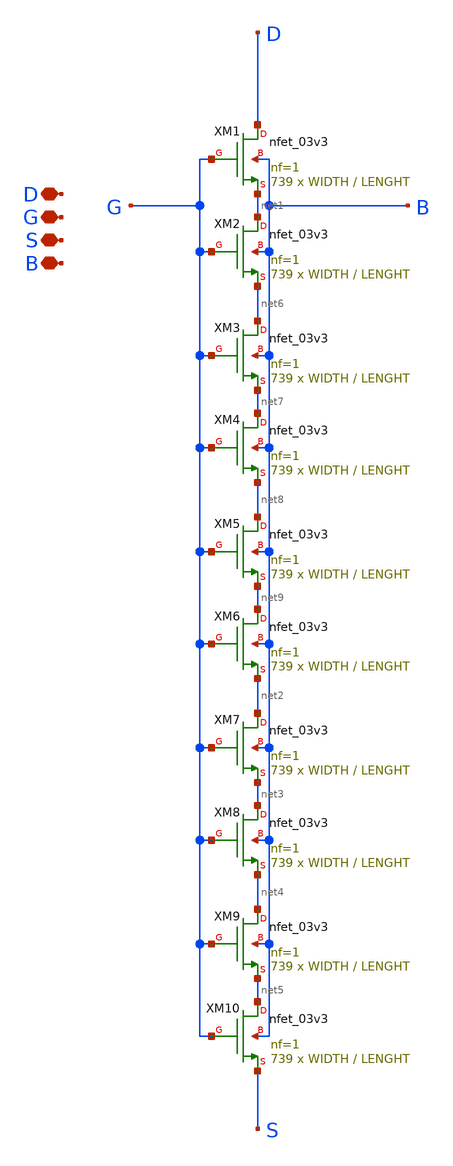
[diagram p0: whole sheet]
** sch_path: New_Extraction/Association/M2_ass.sch
**.subckt M2_ass D G S B
*.iopin D
*.iopin G
*.iopin S
*.iopin B
XM1 D G net1 B nfet_03v3 L=LENGHT W=WIDTH nf=1 ad='int((nf+1)/2) * W/nf * 0.18u' as='int((nf+2)/2) * W/nf * 0.18u'
+ pd='2*int((nf+1)/2) * (W/nf + 0.18u)' ps='2*int((nf+2)/2) * (W/nf + 0.18u)' nrd='0.18u / W' nrs='0.18u / W'
+ sa=0 sb=0 sd=0 m=739
XM2 net1 G net6 B nfet_03v3 L=LENGHT W=WIDTH nf=1 ad='int((nf+1)/2) * W/nf * 0.18u' as='int((nf+2)/2) * W/nf * 0.18u'
+ pd='2*int((nf+1)/2) * (W/nf + 0.18u)' ps='2*int((nf+2)/2) * (W/nf + 0.18u)' nrd='0.18u / W' nrs='0.18u / W'
+ sa=0 sb=0 sd=0 m=739
XM3 net6 G net7 B nfet_03v3 L=LENGHT W=WIDTH nf=1 ad='int((nf+1)/2) * W/nf * 0.18u' as='int((nf+2)/2) * W/nf * 0.18u'
+ pd='2*int((nf+1)/2) * (W/nf + 0.18u)' ps='2*int((nf+2)/2) * (W/nf + 0.18u)' nrd='0.18u / W' nrs='0.18u / W'
+ sa=0 sb=0 sd=0 m=739
XM4 net7 G net8 B nfet_03v3 L=LENGHT W=WIDTH nf=1 ad='int((nf+1)/2) * W/nf * 0.18u' as='int((nf+2)/2) * W/nf * 0.18u'
+ pd='2*int((nf+1)/2) * (W/nf + 0.18u)' ps='2*int((nf+2)/2) * (W/nf + 0.18u)' nrd='0.18u / W' nrs='0.18u / W'
+ sa=0 sb=0 sd=0 m=739
XM5 net8 G net9 B nfet_03v3 L=LENGHT W=WIDTH nf=1 ad='int((nf+1)/2) * W/nf * 0.18u' as='int((nf+2)/2) * W/nf * 0.18u'
+ pd='2*int((nf+1)/2) * (W/nf + 0.18u)' ps='2*int((nf+2)/2) * (W/nf + 0.18u)' nrd='0.18u / W' nrs='0.18u / W'
+ sa=0 sb=0 sd=0 m=739
XM6 net9 G net2 B nfet_03v3 L=LENGHT W=WIDTH nf=1 ad='int((nf+1)/2) * W/nf * 0.18u' as='int((nf+2)/2) * W/nf * 0.18u'
+ pd='2*int((nf+1)/2) * (W/nf + 0.18u)' ps='2*int((nf+2)/2) * (W/nf + 0.18u)' nrd='0.18u / W' nrs='0.18u / W'
+ sa=0 sb=0 sd=0 m=739
XM7 net2 G net3 B nfet_03v3 L=LENGHT W=WIDTH nf=1 ad='int((nf+1)/2) * W/nf * 0.18u' as='int((nf+2)/2) * W/nf * 0.18u'
+ pd='2*int((nf+1)/2) * (W/nf + 0.18u)' ps='2*int((nf+2)/2) * (W/nf + 0.18u)' nrd='0.18u / W' nrs='0.18u / W'
+ sa=0 sb=0 sd=0 m=739
XM8 net3 G net4 B nfet_03v3 L=LENGHT W=WIDTH nf=1 ad='int((nf+1)/2) * W/nf * 0.18u' as='int((nf+2)/2) * W/nf * 0.18u'
+ pd='2*int((nf+1)/2) * (W/nf + 0.18u)' ps='2*int((nf+2)/2) * (W/nf + 0.18u)' nrd='0.18u / W' nrs='0.18u / W'
+ sa=0 sb=0 sd=0 m=739
XM9 net4 G net5 B nfet_03v3 L=LENGHT W=WIDTH nf=1 ad='int((nf+1)/2) * W/nf * 0.18u' as='int((nf+2)/2) * W/nf * 0.18u'
+ pd='2*int((nf+1)/2) * (W/nf + 0.18u)' ps='2*int((nf+2)/2) * (W/nf + 0.18u)' nrd='0.18u / W' nrs='0.18u / W'
+ sa=0 sb=0 sd=0 m=739
XM10 net5 G S B nfet_03v3 L=LENGHT W=WIDTH nf=1 ad='int((nf+1)/2) * W/nf * 0.18u' as='int((nf+2)/2) * W/nf * 0.18u'
+ pd='2*int((nf+1)/2) * (W/nf + 0.18u)' ps='2*int((nf+2)/2) * (W/nf + 0.18u)' nrd='0.18u / W' nrs='0.18u / W'
+ sa=0 sb=0 sd=0 m=739
**.ends
.end
